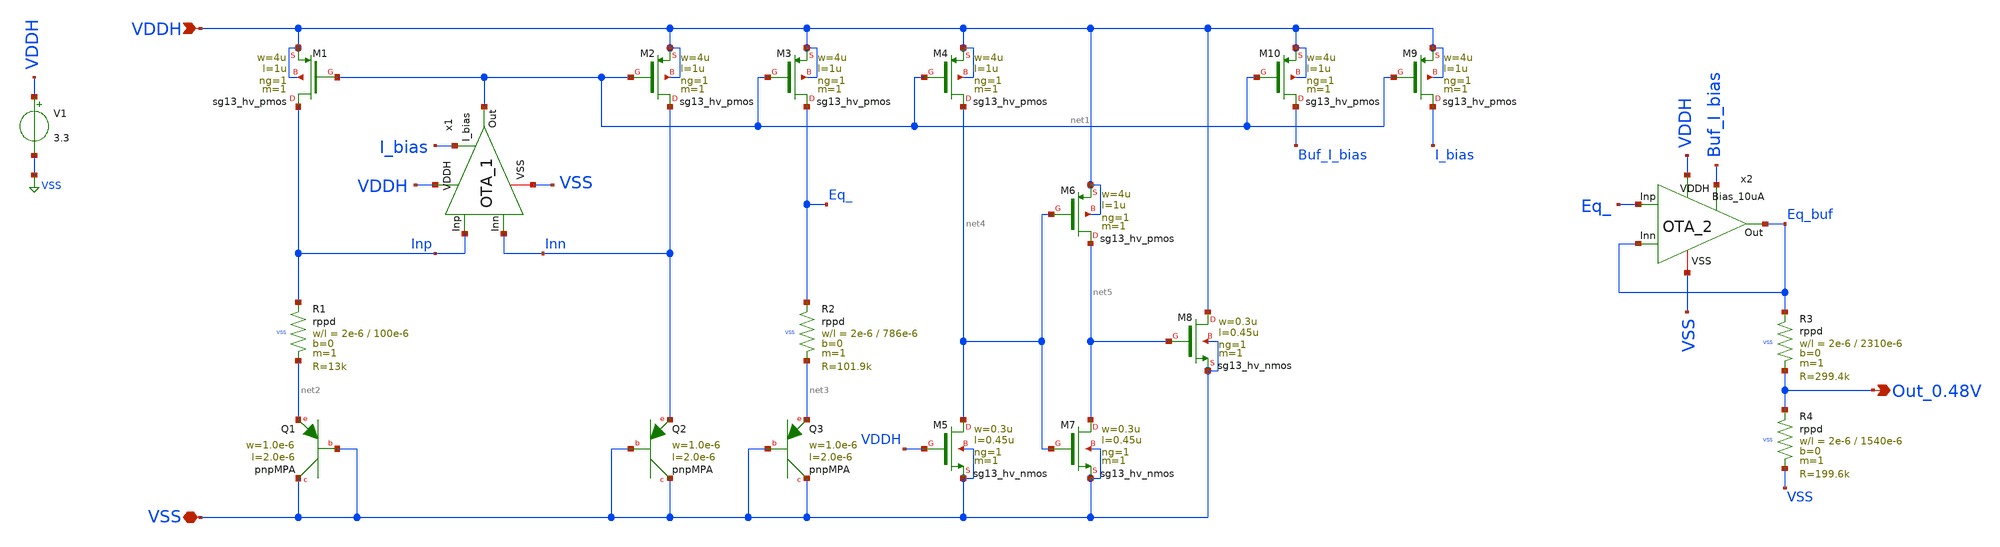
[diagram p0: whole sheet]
** sch_path: sar_adc/xschem/blocks/bandgap/0.48v_bandgap_tb.sch
**.subckt 0.48v_bandgap_tb VDDH VSS Out_0.48V
*.ipin VDDH
*.iopin VSS
*.opin Out_0.48V
XM1 Inp net1 VDDH VDDH sg13_hv_pmos w=4u l=1u ng=1 m=1 mm_ok=1
x1 VDDH Inp Inn net1 I_bias VSS OTA_1
XM2 Inn net1 VDDH VDDH sg13_hv_pmos w=4u l=1u ng=1 m=1 mm_ok=1
XR1 Inp net2 VSS rppd w=2e-6 l=100e-6 m=1 b=0 mm_ok=1
XQ1 VSS VSS net2 pnpMPA a=2p p=6u m=8
XQ2 VSS VSS Inn pnpMPA a=2p p=6u m=1
V1 VDDH VSS 3.3
XM3 Eq_ net1 VDDH VDDH sg13_hv_pmos w=4u l=1u ng=1 m=1 mm_ok=1
XQ3 VSS VSS net3 pnpMPA a=2p p=6u m=1
XR2 Eq_ net3 VSS rppd w=2e-6 l=786e-6 m=1 b=0 mm_ok=1
XM4 net4 net1 VDDH VDDH sg13_hv_pmos w=4u l=1u ng=1 m=1 mm_ok=1
XM5 net4 VDDH VSS VSS sg13_hv_nmos w=0.3u l=0.45u ng=1 m=1 mm_ok=1
XM6 net5 net4 VDDH VDDH sg13_hv_pmos w=4u l=1u ng=1 m=1 mm_ok=1
XM7 net5 net4 VSS VSS sg13_hv_nmos w=0.3u l=0.45u ng=1 m=1 mm_ok=1
XM8 VDDH net5 VSS VSS sg13_hv_nmos w=0.3u l=0.45u ng=1 m=1 mm_ok=1
XM9 I_bias net1 VDDH VDDH sg13_hv_pmos w=4u l=1u ng=1 m=1 mm_ok=1
x2 VDDH Eq_buf Eq_buf Eq_ Buf_I_bias VSS OTA_2
XR3 Eq_buf Out_0.48V VSS rppd w=2e-6 l=2310e-6 m=1 b=0 mm_ok=1
XR4 Out_0.48V VSS VSS rppd w=2e-6 l=1540e-6 m=1 b=0 mm_ok=1
XM10 Buf_I_bias net1 VDDH VDDH sg13_hv_pmos w=4u l=1u ng=1 m=1 mm_ok=1
**** begin user architecture code

.lib $::SG13G2_MODELS/cornerMOShv.lib mos_tt
.lib $::SG13G2_MODELS/cornerRES.lib res_typ
.lib $::SG13G2_MODELS/cornerCAP.lib cap_typ
.lib $::SG13G2_MODELS/cornerHBT.lib hbt_typ



.control
 save all

set temp=27
op
echo === OP node voltages ===
print v(Inp) v(net2) v(net3) v(net4) v(Inn) v(eq_)
print n.xr1.nr1#i1 n.xr1.nr1#i2
print n.xm1.nsg13_hv_pmos#di
print n.xm3.nsg13_hv_pmos#di

dc temp -40 125 1

* Correct nodes after netlist analysis:
* Inn  = Q2 emitter = Vbe (CTAT reference)
* net2 = top of XR1 = OTA.Inp (tracks Inn when loop closed)
* net3 = bottom of XR1 = Q1 emitter
* ΔVbe = net2 - net3

let vbe   = inn
let vdvbe = net2 - net3
let veq   = eq_
let vnet4 = net4

* Vbe CTAT stats
let vbe_max = vecmax(vbe)
let vbe_min = vecmin(vbe)
let vbe_nom = mean(vbe)
let tc_vbe  = ((vbe_max - vbe_min) / vbe_nom) * 1e6 / 165

* ΔVbe PTAT stats
let vr_max = vecmax(vdvbe)
let vr_min = vecmin(vdvbe)
let vr_nom = mean(vdvbe)
let tc_vr  = ((vr_max - vr_min) / vr_nom) * 1e6 / 165

* PTAT current
let i_ptat    = vdvbe / 13e3
let i_ptat_ua = i_ptat * 1e6

* CATA output
let veq_max = vecmax(veq)
let veq_min = vecmin(veq)
let veq_nom = mean(veq)
let tc_eq   = ((veq_max - veq_min) / veq_nom) * 1e6 / 165

echo === Vbe CTAT (Inn) ===
print vbe_max vbe_min vbe_nom tc_vbe

echo === Delta_Vbe PTAT (net2-net3) ===
print vr_max vr_min vr_nom tc_vr

echo === I_PTAT uA ===
print vecmax(i_ptat_ua) vecmin(i_ptat_ua) mean(i_ptat_ua)

echo === Eq bandgap output ===
print veq_max veq_min veq_nom tc_eq

echo === net4 Q3 emitter ===
print vecmax(vnet4) vecmin(vnet4) mean(vnet4)

plot inn title 'Vbe vs T (CTAT)'
plot net2 - net3 title 'Delta_Vbe vs T (PTAT)'
plot eq_ title 'Eq bandgap output vs T'
plot i_ptat_ua title 'I_PTAT uA vs T'

wrdata /tmp/bg_inn.txt dc1.inn
wrdata /tmp/bg_eq.txt dc1.eq

echo === Eq bandgap output ===
print veq_max veq_min veq_nom tc_eq

* Better TC calculation — use max deviation from nominal
let veq_center = (veq_max + veq_min) / 2
let tc_eq_pp = (veq_max - veq_min) / veq_center * 1e6 / 165
print tc_eq_pp


print v(Eq_buf)
print v(Out_0.48V)
print n.xr3.nr1#i1

plot v(Out_0.48V)


.endc


**** end user architecture code
**.ends
.GLOBAL VSS
.end
